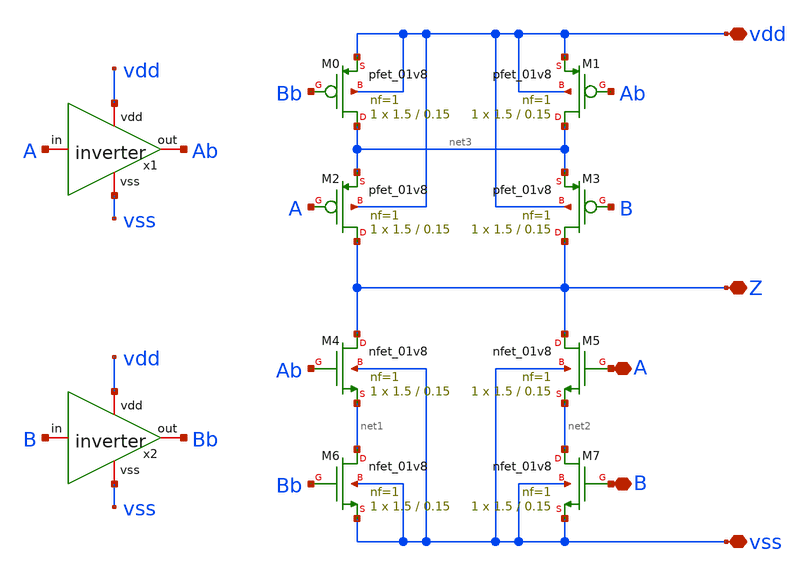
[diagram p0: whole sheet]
** sch_path: designs/xor.sch
**.subckt xor A B vdd Z vss
*.iopin A
*.iopin B
*.iopin vdd
*.iopin Z
*.iopin vss
XM6 net1 Bb vss vss sky130_fd_pr__nfet_01v8 L=0.15 W=1.5 nf=1 ad='int((nf+1)/2) * W/nf * 0.29' as='int((nf+2)/2) * W/nf * 0.29'
+ pd='2*int((nf+1)/2) * (W/nf + 0.29)' ps='2*int((nf+2)/2) * (W/nf + 0.29)' nrd='0.29 / W' nrs='0.29 / W'
+ sa=0 sb=0 sd=0 mult=1 m=1
XM4 Z Ab net1 vss sky130_fd_pr__nfet_01v8 L=0.15 W=1.5 nf=1 ad='int((nf+1)/2) * W/nf * 0.29' as='int((nf+2)/2) * W/nf * 0.29'
+ pd='2*int((nf+1)/2) * (W/nf + 0.29)' ps='2*int((nf+2)/2) * (W/nf + 0.29)' nrd='0.29 / W' nrs='0.29 / W'
+ sa=0 sb=0 sd=0 mult=1 m=1
XM5 Z A net2 vss sky130_fd_pr__nfet_01v8 L=0.15 W=1.5 nf=1 ad='int((nf+1)/2) * W/nf * 0.29' as='int((nf+2)/2) * W/nf * 0.29'
+ pd='2*int((nf+1)/2) * (W/nf + 0.29)' ps='2*int((nf+2)/2) * (W/nf + 0.29)' nrd='0.29 / W' nrs='0.29 / W'
+ sa=0 sb=0 sd=0 mult=1 m=1
XM7 net2 B vss vss sky130_fd_pr__nfet_01v8 L=0.15 W=1.5 nf=1 ad='int((nf+1)/2) * W/nf * 0.29' as='int((nf+2)/2) * W/nf * 0.29'
+ pd='2*int((nf+1)/2) * (W/nf + 0.29)' ps='2*int((nf+2)/2) * (W/nf + 0.29)' nrd='0.29 / W' nrs='0.29 / W'
+ sa=0 sb=0 sd=0 mult=1 m=1
XM0 net3 Bb vdd vdd sky130_fd_pr__pfet_01v8 L=0.15 W=1.5 nf=1 ad='int((nf+1)/2) * W/nf * 0.29' as='int((nf+2)/2) * W/nf * 0.29'
+ pd='2*int((nf+1)/2) * (W/nf + 0.29)' ps='2*int((nf+2)/2) * (W/nf + 0.29)' nrd='0.29 / W' nrs='0.29 / W'
+ sa=0 sb=0 sd=0 mult=1 m=1
XM1 net3 Ab vdd vdd sky130_fd_pr__pfet_01v8 L=0.15 W=1.5 nf=1 ad='int((nf+1)/2) * W/nf * 0.29' as='int((nf+2)/2) * W/nf * 0.29'
+ pd='2*int((nf+1)/2) * (W/nf + 0.29)' ps='2*int((nf+2)/2) * (W/nf + 0.29)' nrd='0.29 / W' nrs='0.29 / W'
+ sa=0 sb=0 sd=0 mult=1 m=1
XM2 Z A net3 vdd sky130_fd_pr__pfet_01v8 L=0.15 W=1.5 nf=1 ad='int((nf+1)/2) * W/nf * 0.29' as='int((nf+2)/2) * W/nf * 0.29'
+ pd='2*int((nf+1)/2) * (W/nf + 0.29)' ps='2*int((nf+2)/2) * (W/nf + 0.29)' nrd='0.29 / W' nrs='0.29 / W'
+ sa=0 sb=0 sd=0 mult=1 m=1
XM3 Z B net3 vdd sky130_fd_pr__pfet_01v8 L=0.15 W=1.5 nf=1 ad='int((nf+1)/2) * W/nf * 0.29' as='int((nf+2)/2) * W/nf * 0.29'
+ pd='2*int((nf+1)/2) * (W/nf + 0.29)' ps='2*int((nf+2)/2) * (W/nf + 0.29)' nrd='0.29 / W' nrs='0.29 / W'
+ sa=0 sb=0 sd=0 mult=1 m=1
x1 vdd Ab A vss inverter
x2 vdd Bb B vss inverter
**.ends

* expanding   symbol:  /foss/designs/inverter.sym # of pins=4
** sym_path: designs/inverter.sym
** sch_path: designs/inverter.sch
.subckt inverter vdd out in vss
*.iopin out
*.iopin vss
*.iopin vdd
*.iopin in
XM2 out in vss vss sky130_fd_pr__nfet_01v8 L=0.15 W=0.75 nf=1 ad='int((nf+1)/2) * W/nf * 0.29' as='int((nf+2)/2) * W/nf * 0.29'
+ pd='2*int((nf+1)/2) * (W/nf + 0.29)' ps='2*int((nf+2)/2) * (W/nf + 0.29)' nrd='0.29 / W' nrs='0.29 / W'
+ sa=0 sb=0 sd=0 mult=1 m=1
XM1 out in vdd vdd sky130_fd_pr__pfet_01v8 L=0.15 W=1.5 nf=1 ad='int((nf+1)/2) * W/nf * 0.29' as='int((nf+2)/2) * W/nf * 0.29'
+ pd='2*int((nf+1)/2) * (W/nf + 0.29)' ps='2*int((nf+2)/2) * (W/nf + 0.29)' nrd='0.29 / W' nrs='0.29 / W'
+ sa=0 sb=0 sd=0 mult=1 m=1
.ends

.end
